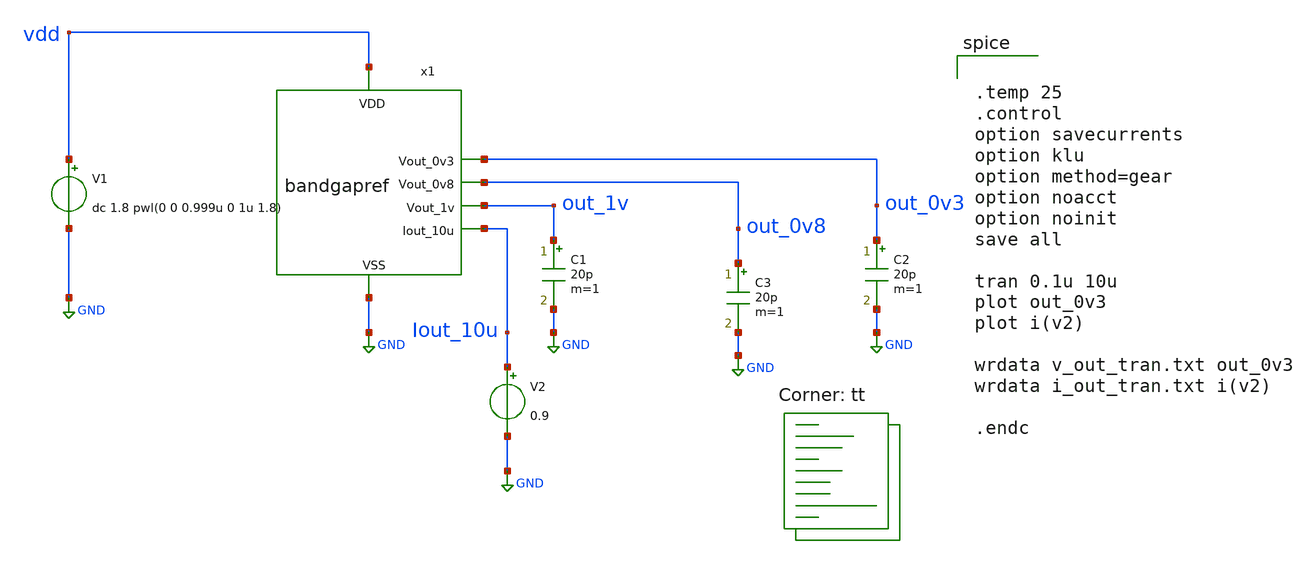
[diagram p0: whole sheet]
** sch_path: bandgapref_tran_tb.sch
**.subckt bandgapref_tran_tb
V1 vdd GND dc 1.8 pwl(0 0 0.999u 0 1u 1.8)
.save i(v1)
x1 vdd out_0v3 GND out_1v out_0v8 Iout_10u bandgapref
C1 out_1v GND 20p m=1
C2 out_0v3 GND 20p m=1
C3 out_0v8 GND 20p m=1
V2 Iout_10u GND 0.9
.save i(v2)
**** begin user architecture code
.lib $::SKYWATER_MODELS/sky130.lib.spice tt


.temp 25
.control
option savecurrents
option klu
option method=gear
option noacct
option noinit
save all

tran 0.1u 10u
plot out_0v3
plot i(v2)

wrdata v_out_tran.txt out_0v3
wrdata i_out_tran.txt i(v2)

.endc

**** end user architecture code
**.ends
.GLOBAL GND
.end
